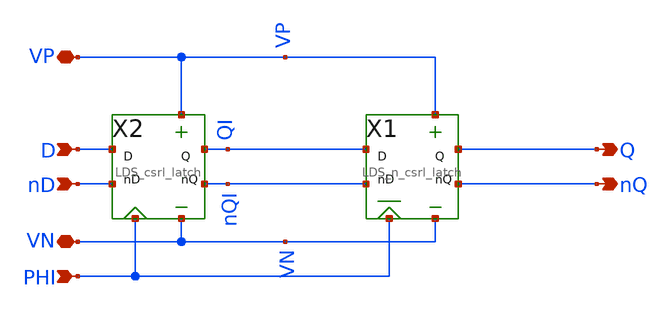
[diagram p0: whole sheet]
** sch_path: LDS/LDS_posdff.sch
**.subckt LDS_posdff VP D Q nD PHI nQ VN
*.iopin VP
*.ipin D
*.opin Q
*.ipin nD
*.ipin PHI
*.opin nQ
*.iopin VN
X2 VN VP nQI QI PHI nD D LDS_csrl_latch
X1 VN VP nQ Q PHI nQI QI LDS_n_csrl_latch
**.ends

* expanding   symbol:  /home/madvlsi/Documents/dpll/LDS/LDS_csrl_latch.sym # of pins=7
** sym_path: LDS/LDS_csrl_latch.sym
** sch_path: LDS/LDS_csrl_latch.sch
.subckt LDS_csrl_latch VN VP nQ Q PHI nD D
*.ipin nD
*.ipin D
*.opin Q
*.opin nQ
*.ipin PHI
*.iopin VP
*.iopin VN
XM7 net3 D VN VN sky130_fd_pr__nfet_01v8 L={dff_len} W={dff_wid} nf=1 ad='int((nf+1)/2) * W/nf * 0.29'
+ as='int((nf+2)/2) * W/nf * 0.29' pd='2*int((nf+1)/2) * (W/nf + 0.29)' ps='2*int((nf+2)/2) * (W/nf + 0.29)'
+ nrd='0.29 / W' nrs='0.29 / W' sa=0 sb=0 sd=0 mult=1 m=1
XM8 VN PHI net3 VN sky130_fd_pr__nfet_01v8 L={dff_len} W={dff_wid} nf=1 ad='int((nf+1)/2) * W/nf * 0.29'
+ as='int((nf+2)/2) * W/nf * 0.29' pd='2*int((nf+1)/2) * (W/nf + 0.29)' ps='2*int((nf+2)/2) * (W/nf + 0.29)'
+ nrd='0.29 / W' nrs='0.29 / W' sa=0 sb=0 sd=0 mult=1 m=1
XM9 nQ Q net3 VN sky130_fd_pr__nfet_01v8 L={dff_len} W={dff_wid} nf=1 ad='int((nf+1)/2) * W/nf * 0.29'
+ as='int((nf+2)/2) * W/nf * 0.29' pd='2*int((nf+1)/2) * (W/nf + 0.29)' ps='2*int((nf+2)/2) * (W/nf + 0.29)'
+ nrd='0.29 / W' nrs='0.29 / W' sa=0 sb=0 sd=0 mult=1 m=1
XM10 VN nD net2 VN sky130_fd_pr__nfet_01v8 L={dff_len} W={dff_wid} nf=1 ad='int((nf+1)/2) * W/nf * 0.29'
+ as='int((nf+2)/2) * W/nf * 0.29' pd='2*int((nf+1)/2) * (W/nf + 0.29)' ps='2*int((nf+2)/2) * (W/nf + 0.29)'
+ nrd='0.29 / W' nrs='0.29 / W' sa=0 sb=0 sd=0 mult=1 m=1
XM11 VN PHI net2 VN sky130_fd_pr__nfet_01v8 L={dff_len} W={dff_wid} nf=1 ad='int((nf+1)/2) * W/nf * 0.29'
+ as='int((nf+2)/2) * W/nf * 0.29' pd='2*int((nf+1)/2) * (W/nf + 0.29)' ps='2*int((nf+2)/2) * (W/nf + 0.29)'
+ nrd='0.29 / W' nrs='0.29 / W' sa=0 sb=0 sd=0 mult=1 m=1
XM12 Q nQ net2 VN sky130_fd_pr__nfet_01v8 L={dff_len} W={dff_wid} nf=1 ad='int((nf+1)/2) * W/nf * 0.29'
+ as='int((nf+2)/2) * W/nf * 0.29' pd='2*int((nf+1)/2) * (W/nf + 0.29)' ps='2*int((nf+2)/2) * (W/nf + 0.29)'
+ nrd='0.29 / W' nrs='0.29 / W' sa=0 sb=0 sd=0 mult=1 m=1
XM19 net1 nD VP VP sky130_fd_pr__pfet_01v8 L={dff_len} W={dff_wid} nf=1 ad='int((nf+1)/2) * W/nf * 0.29'
+ as='int((nf+2)/2) * W/nf * 0.29' pd='2*int((nf+1)/2) * (W/nf + 0.29)' ps='2*int((nf+2)/2) * (W/nf + 0.29)'
+ nrd='0.29 / W' nrs='0.29 / W' sa=0 sb=0 sd=0 mult=1 m=1
XM20 Q PHI net1 VP sky130_fd_pr__pfet_01v8 L={dff_len} W={dff_wid} nf=1 ad='int((nf+1)/2) * W/nf * 0.29'
+ as='int((nf+2)/2) * W/nf * 0.29' pd='2*int((nf+1)/2) * (W/nf + 0.29)' ps='2*int((nf+2)/2) * (W/nf + 0.29)'
+ nrd='0.29 / W' nrs='0.29 / W' sa=0 sb=0 sd=0 mult=1 m=1
XM21 VP nQ Q VP sky130_fd_pr__pfet_01v8 L={dff_len} W={dff_wid} nf=1 ad='int((nf+1)/2) * W/nf * 0.29'
+ as='int((nf+2)/2) * W/nf * 0.29' pd='2*int((nf+1)/2) * (W/nf + 0.29)' ps='2*int((nf+2)/2) * (W/nf + 0.29)'
+ nrd='0.29 / W' nrs='0.29 / W' sa=0 sb=0 sd=0 mult=1 m=1
XM22 VP D net4 VP sky130_fd_pr__pfet_01v8 L={dff_len} W={dff_wid} nf=1 ad='int((nf+1)/2) * W/nf * 0.29'
+ as='int((nf+2)/2) * W/nf * 0.29' pd='2*int((nf+1)/2) * (W/nf + 0.29)' ps='2*int((nf+2)/2) * (W/nf + 0.29)'
+ nrd='0.29 / W' nrs='0.29 / W' sa=0 sb=0 sd=0 mult=1 m=1
XM23 nQ PHI net4 VP sky130_fd_pr__pfet_01v8 L={dff_len} W={dff_wid} nf=1 ad='int((nf+1)/2) * W/nf * 0.29'
+ as='int((nf+2)/2) * W/nf * 0.29' pd='2*int((nf+1)/2) * (W/nf + 0.29)' ps='2*int((nf+2)/2) * (W/nf + 0.29)'
+ nrd='0.29 / W' nrs='0.29 / W' sa=0 sb=0 sd=0 mult=1 m=1
XM24 VP Q nQ VP sky130_fd_pr__pfet_01v8 L={dff_len} W={dff_wid} nf=1 ad='int((nf+1)/2) * W/nf * 0.29'
+ as='int((nf+2)/2) * W/nf * 0.29' pd='2*int((nf+1)/2) * (W/nf + 0.29)' ps='2*int((nf+2)/2) * (W/nf + 0.29)'
+ nrd='0.29 / W' nrs='0.29 / W' sa=0 sb=0 sd=0 mult=1 m=1
**** begin user architecture code


.param dff_wid=0.5 dff_len=0.5


**** end user architecture code
.ends


* expanding   symbol:  /home/madvlsi/Documents/dpll/LDS/LDS_n_csrl_latch.sym # of pins=7
** sym_path: LDS/LDS_n_csrl_latch.sym
** sch_path: LDS/LDS_n_csrl_latch.sch
.subckt LDS_n_csrl_latch VN VP nQ Q PHI nD D
*.ipin D
*.ipin nD
*.opin nQ
*.opin Q
*.ipin PHI
*.iopin VP
*.iopin VN
XM1 VN nD net3 VN sky130_fd_pr__nfet_01v8 L={dff_len} W={dff_wid} nf=1 ad='int((nf+1)/2) * W/nf * 0.29'
+ as='int((nf+2)/2) * W/nf * 0.29' pd='2*int((nf+1)/2) * (W/nf + 0.29)' ps='2*int((nf+2)/2) * (W/nf + 0.29)'
+ nrd='0.29 / W' nrs='0.29 / W' sa=0 sb=0 sd=0 mult=1 m=1
XM2 net3 PHI Q VN sky130_fd_pr__nfet_01v8 L={dff_len} W={dff_wid} nf=1 ad='int((nf+1)/2) * W/nf * 0.29'
+ as='int((nf+2)/2) * W/nf * 0.29' pd='2*int((nf+1)/2) * (W/nf + 0.29)' ps='2*int((nf+2)/2) * (W/nf + 0.29)'
+ nrd='0.29 / W' nrs='0.29 / W' sa=0 sb=0 sd=0 mult=1 m=1
XM3 VN nQ Q VN sky130_fd_pr__nfet_01v8 L={dff_len} W={dff_wid} nf=1 ad='int((nf+1)/2) * W/nf * 0.29'
+ as='int((nf+2)/2) * W/nf * 0.29' pd='2*int((nf+1)/2) * (W/nf + 0.29)' ps='2*int((nf+2)/2) * (W/nf + 0.29)'
+ nrd='0.29 / W' nrs='0.29 / W' sa=0 sb=0 sd=0 mult=1 m=1
XM4 net1 D VN VN sky130_fd_pr__nfet_01v8 L={dff_len} W={dff_wid} nf=1 ad='int((nf+1)/2) * W/nf * 0.29'
+ as='int((nf+2)/2) * W/nf * 0.29' pd='2*int((nf+1)/2) * (W/nf + 0.29)' ps='2*int((nf+2)/2) * (W/nf + 0.29)'
+ nrd='0.29 / W' nrs='0.29 / W' sa=0 sb=0 sd=0 mult=1 m=1
XM5 net1 PHI nQ VN sky130_fd_pr__nfet_01v8 L={dff_len} W={dff_wid} nf=1 ad='int((nf+1)/2) * W/nf * 0.29'
+ as='int((nf+2)/2) * W/nf * 0.29' pd='2*int((nf+1)/2) * (W/nf + 0.29)' ps='2*int((nf+2)/2) * (W/nf + 0.29)'
+ nrd='0.29 / W' nrs='0.29 / W' sa=0 sb=0 sd=0 mult=1 m=1
XM6 VN Q nQ VN sky130_fd_pr__nfet_01v8 L={dff_len} W={dff_wid} nf=1 ad='int((nf+1)/2) * W/nf * 0.29'
+ as='int((nf+2)/2) * W/nf * 0.29' pd='2*int((nf+1)/2) * (W/nf + 0.29)' ps='2*int((nf+2)/2) * (W/nf + 0.29)'
+ nrd='0.29 / W' nrs='0.29 / W' sa=0 sb=0 sd=0 mult=1 m=1
XM13 VP D net2 VP sky130_fd_pr__pfet_01v8 L={dff_len} W={dff_wid} nf=1 ad='int((nf+1)/2) * W/nf * 0.29'
+ as='int((nf+2)/2) * W/nf * 0.29' pd='2*int((nf+1)/2) * (W/nf + 0.29)' ps='2*int((nf+2)/2) * (W/nf + 0.29)'
+ nrd='0.29 / W' nrs='0.29 / W' sa=0 sb=0 sd=0 mult=1 m=1
XM14 net2 PHI VP VP sky130_fd_pr__pfet_01v8 L={dff_len} W={dff_wid} nf=1 ad='int((nf+1)/2) * W/nf * 0.29'
+ as='int((nf+2)/2) * W/nf * 0.29' pd='2*int((nf+1)/2) * (W/nf + 0.29)' ps='2*int((nf+2)/2) * (W/nf + 0.29)'
+ nrd='0.29 / W' nrs='0.29 / W' sa=0 sb=0 sd=0 mult=1 m=1
XM15 nQ Q net2 VP sky130_fd_pr__pfet_01v8 L={dff_len} W={dff_wid} nf=1 ad='int((nf+1)/2) * W/nf * 0.29'
+ as='int((nf+2)/2) * W/nf * 0.29' pd='2*int((nf+1)/2) * (W/nf + 0.29)' ps='2*int((nf+2)/2) * (W/nf + 0.29)'
+ nrd='0.29 / W' nrs='0.29 / W' sa=0 sb=0 sd=0 mult=1 m=1
XM16 net4 nD VP VP sky130_fd_pr__pfet_01v8 L={dff_len} W={dff_wid} nf=1 ad='int((nf+1)/2) * W/nf * 0.29'
+ as='int((nf+2)/2) * W/nf * 0.29' pd='2*int((nf+1)/2) * (W/nf + 0.29)' ps='2*int((nf+2)/2) * (W/nf + 0.29)'
+ nrd='0.29 / W' nrs='0.29 / W' sa=0 sb=0 sd=0 mult=1 m=1
XM17 net4 PHI VP VP sky130_fd_pr__pfet_01v8 L={dff_len} W={dff_wid} nf=1 ad='int((nf+1)/2) * W/nf * 0.29'
+ as='int((nf+2)/2) * W/nf * 0.29' pd='2*int((nf+1)/2) * (W/nf + 0.29)' ps='2*int((nf+2)/2) * (W/nf + 0.29)'
+ nrd='0.29 / W' nrs='0.29 / W' sa=0 sb=0 sd=0 mult=1 m=1
XM18 Q nQ net4 VP sky130_fd_pr__pfet_01v8 L={dff_len} W={dff_wid} nf=1 ad='int((nf+1)/2) * W/nf * 0.29'
+ as='int((nf+2)/2) * W/nf * 0.29' pd='2*int((nf+1)/2) * (W/nf + 0.29)' ps='2*int((nf+2)/2) * (W/nf + 0.29)'
+ nrd='0.29 / W' nrs='0.29 / W' sa=0 sb=0 sd=0 mult=1 m=1
**** begin user architecture code


.param dff_wid=0.5 dff_len=0.5


**** end user architecture code
.ends

.end
